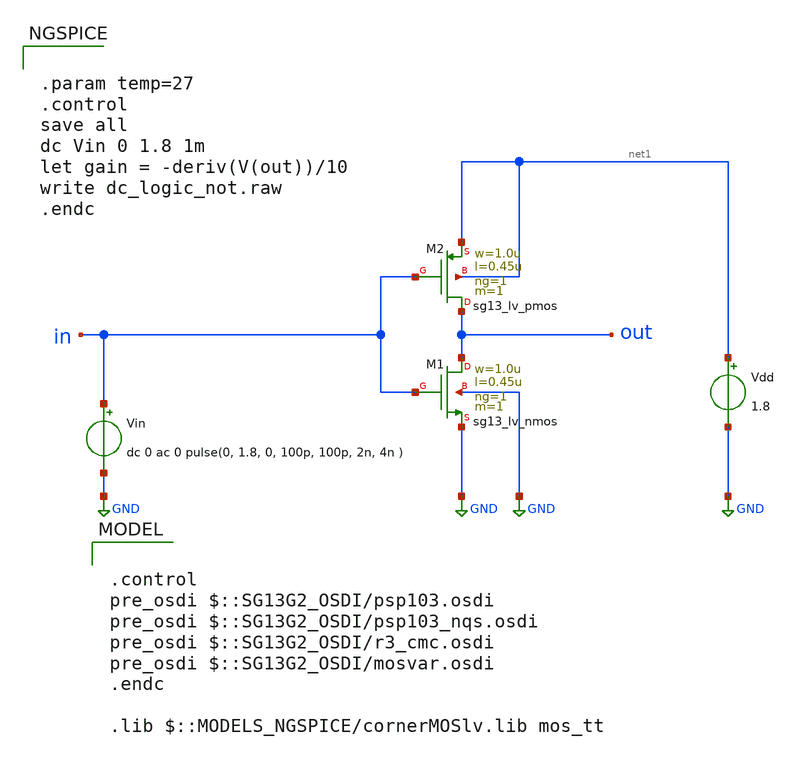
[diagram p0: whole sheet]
** sch_path: ihp-sg13g2/xschem_libs/sg13g2_tests/dc_logic_not/schematic/dc_logic_not.sch
* Copyright 2023 IHP PDK Authors
**.subckt dc_logic_not
Vin in GND dc 0 ac 0 pulse(0, 1.8, 0, 100p, 100p, 2n, 4n )
Vdd net1 GND 1.8
XM1 out in GND GND sg13_lv_nmos w=1.0u l=0.45u ng=1 m=1 mm_ok=1
XM2 out in net1 net1 sg13_lv_pmos w=1.0u l=0.45u ng=1 m=1 mm_ok=1
**** begin user architecture code

.control
pre_osdi $::SG13G2_OSDI/psp103.osdi
pre_osdi $::SG13G2_OSDI/psp103_nqs.osdi
pre_osdi $::SG13G2_OSDI/r3_cmc.osdi
pre_osdi $::SG13G2_OSDI/mosvar.osdi
.endc

.lib $::MODELS_NGSPICE/cornerMOSlv.lib mos_tt



.param temp=27
.control
save all
dc Vin 0 1.8 1m
let gain = -deriv(V(out))/10
write dc_logic_not.raw
.endc


**** end user architecture code
**.ends
.GLOBAL GND
.end
